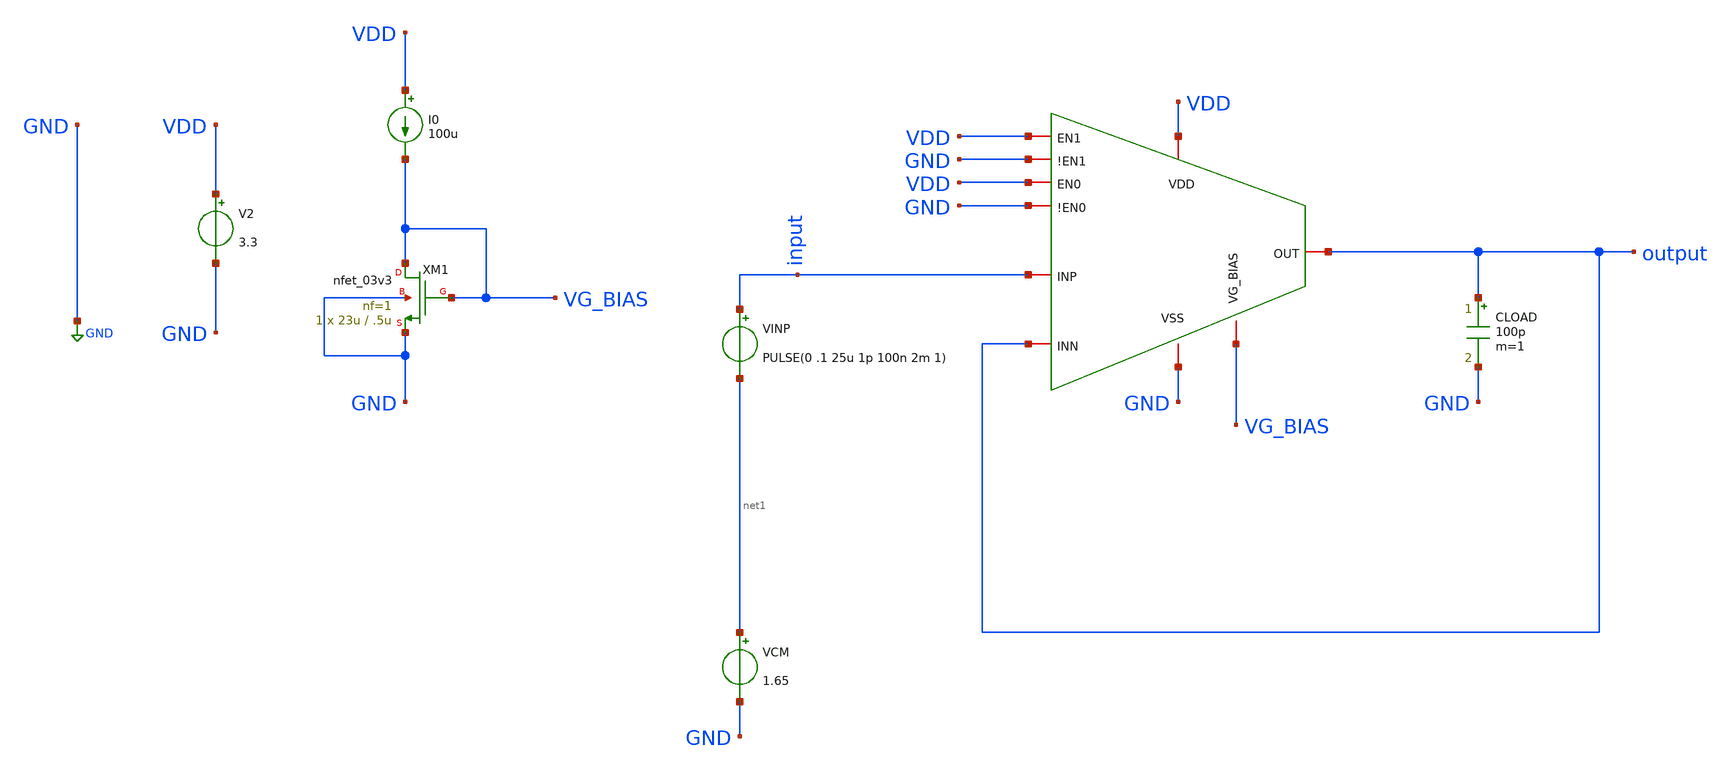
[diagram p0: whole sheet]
** sch_path: designs/libs/old_files/old_amps/ota_folded_cascode/programmable_tran_small_step_tb.sch
**.subckt programmable_tran_small_step_tb
x1 VDD VDD GND GND VDD GND output input output VG_BIAS programmable_folded
XM1 VG_BIAS VG_BIAS GND GND nfet_03v3 L=.5u W=23u nf=1 ad='int((nf+1)/2) * W/nf * 0.18u' as='int((nf+2)/2) * W/nf * 0.18u'
+ pd='2*int((nf+1)/2) * (W/nf + 0.18u)' ps='2*int((nf+2)/2) * (W/nf + 0.18u)' nrd='0.18u / W' nrs='0.18u / W'
+ sa=0 sb=0 sd=0 m=1
I0 VDD VG_BIAS 100u
V2 VDD GND 3.3
CLOAD output GND 100p m=1
VINP input net1 PULSE(0 .1 25u 1p 100n 2m 1)
VCM net1 GND 1.65
**** begin user architecture code

.include $::180MCU_MODELS/design.ngspice
.lib $::180MCU_MODELS/sm141064.ngspice typical



.control
tran 1n 50u
meas tran v_input find v(input) at=40u
meas tran v_output find v(output) at=40u
let v_error = v_input - v_output
print v_error

meas tran vpeak max v(output) from=10u to=50u
meas tran vfinal find v(output) at=40u

let target_low = vfinal * 0.999
meas tran settle_01 when v(output) = target_low rise = last

print v_input v_output
print vpeak vfinal
print settle_01

plot v(input) v(output)
plot v(output) - v(input)
.endc


**** end user architecture code
**.ends
.GLOBAL GND
.end
